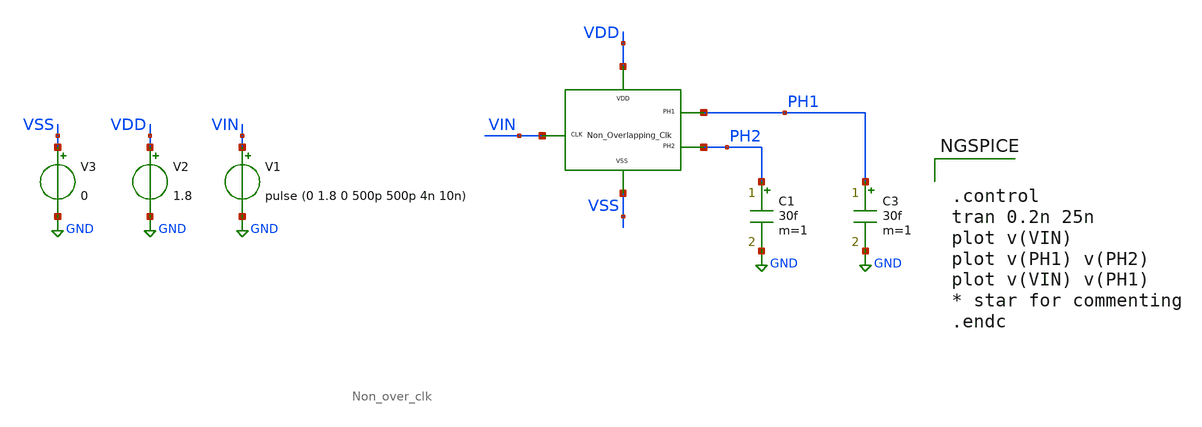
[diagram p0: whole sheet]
** sch_path: xschem/DC_DC_Converter_xschem/OTHERS/DC_DC_Converter_V7/Non_Overlap_Clk/Non_over_clk_TB_V2.sch
**.subckt Non_over_clk_TB_V2
V1 VIN GND pulse (0 1.8 0 500p 500p 4n 10n)
C3 PH1 GND 30f m=1
C1 PH2 GND 30f m=1
V2 VDD GND 1.8
V3 VSS GND 0
x1 VDD VIN PH1 VSS PH2 Non_over_clk
**** begin user architecture code


.control
tran 0.2n 25n
plot v(VIN)
plot v(PH1) v(PH2)
plot v(VIN) v(PH1)
* star for commenting
.endc

** manual skywater pdks install (with patches applied)
* .lib $::SKYWATER_MODELS/models/sky130.lib.spice tt

** opencircuitdesign pdks install
.lib $::SKYWATER_MODELS/sky130.lib.spice tt
.include $::SKYWATER_STDCELLS/sky130_fd_sc_hd.spice

**** end user architecture code
**.ends
.GLOBAL GND
.end
